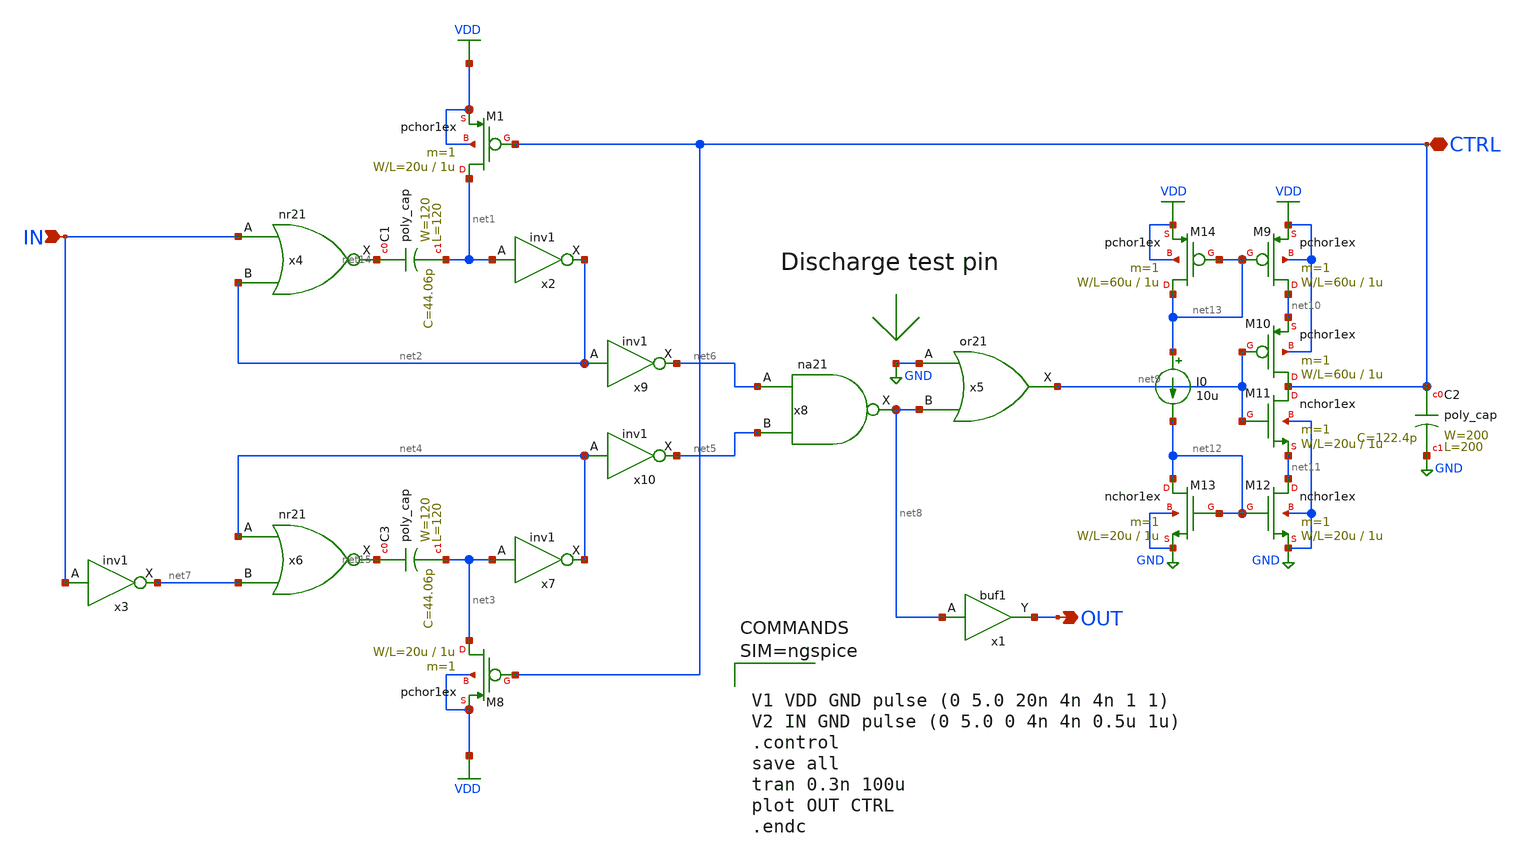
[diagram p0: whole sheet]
** sch_path: member_project/3zki/clkdb_concept.sch
**.subckt clkdb_concept IN OUT CTRL
*.ipin IN
*.opin OUT
*.iopin CTRL
x4 IN net2 VDD GND net14 nr21
C1 net14 net1 poly_cap W=120 L=120
M1 net1 CTRL VDD VDD pchor1ex L=1u W=20u m=1
C2 CTRL GND poly_cap W=200 L=200
x1 net8 VDD GND OUT buf1
x2 net1 VDD GND net2 inv1
x5 GND net8 VDD GND net9 or21
x3 IN VDD GND net7 inv1
x6 net4 net7 VDD GND net15 nr21
C3 net15 net3 poly_cap W=120 L=120
x7 net3 VDD GND net4 inv1
M8 net3 CTRL VDD VDD pchor1ex L=1u W=20u m=1
x9 net2 VDD GND net6 inv1
x10 net4 VDD GND net5 inv1
x8 net6 net5 VDD GND net8 na21
M9 net10 net13 VDD VDD pchor1ex L=1u W=60u m=1
M10 CTRL net9 net10 VDD pchor1ex L=1u W=60u m=1
M11 CTRL net9 net11 GND nchor1ex L=1u W=20u m=1
M12 net11 net12 GND GND nchor1ex L=1u W=20u m=1
M13 net12 net12 GND GND nchor1ex L=1u W=20u m=1
M14 net13 net13 VDD VDD pchor1ex L=1u W=60u m=1
I0 net13 net12 10u
**** begin user architecture code
 .include $::LIB/mos.lib
.include $::LIB/passive.lib
.include $::LIB/diode.lib



V1 VDD GND pulse (0 5.0 20n 4n 4n 1 1)
V2 IN GND pulse (0 5.0 0 4n 4n 0.5u 1u)
.control
save all
tran 0.3n 100u
plot OUT CTRL
.endc



**** end user architecture code
**.ends
.GLOBAL GND
.GLOBAL VDD
.end
